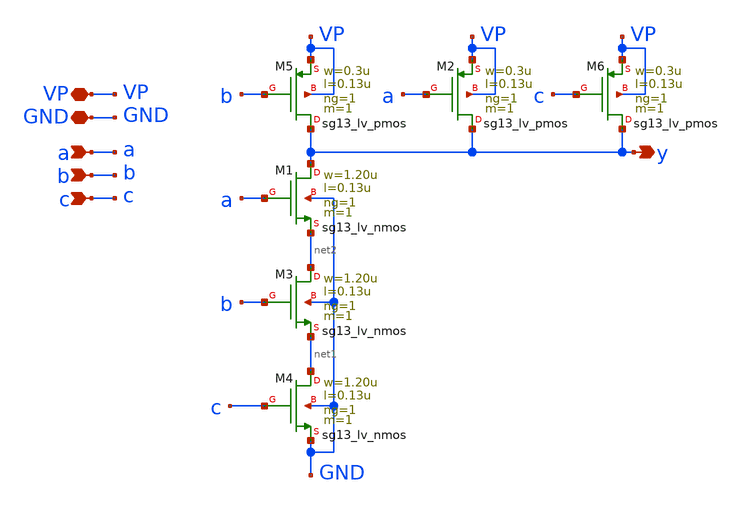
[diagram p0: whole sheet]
** sch_path: schematics/divider/schematics/NAND_3in_x3.sch
**.subckt NAND_3in_x3 y GND a VP b c
*.opin y
*.iopin GND
*.ipin a
*.iopin VP
*.ipin b
*.ipin c
XM1 y a net2 GND sg13_lv_nmos w=1.20u l=0.13u ng=1 m=1 mm_ok=1
XM5 y b VP VP sg13_lv_pmos w=0.3u l=0.13u ng=1 m=1 mm_ok=1
XM3 net2 b net1 GND sg13_lv_nmos w=1.20u l=0.13u ng=1 m=1 mm_ok=1
XM4 net1 c GND GND sg13_lv_nmos w=1.20u l=0.13u ng=1 m=1 mm_ok=1
XM2 y a VP VP sg13_lv_pmos w=0.3u l=0.13u ng=1 m=1 mm_ok=1
XM6 y c VP VP sg13_lv_pmos w=0.3u l=0.13u ng=1 m=1 mm_ok=1
**.ends
.end
